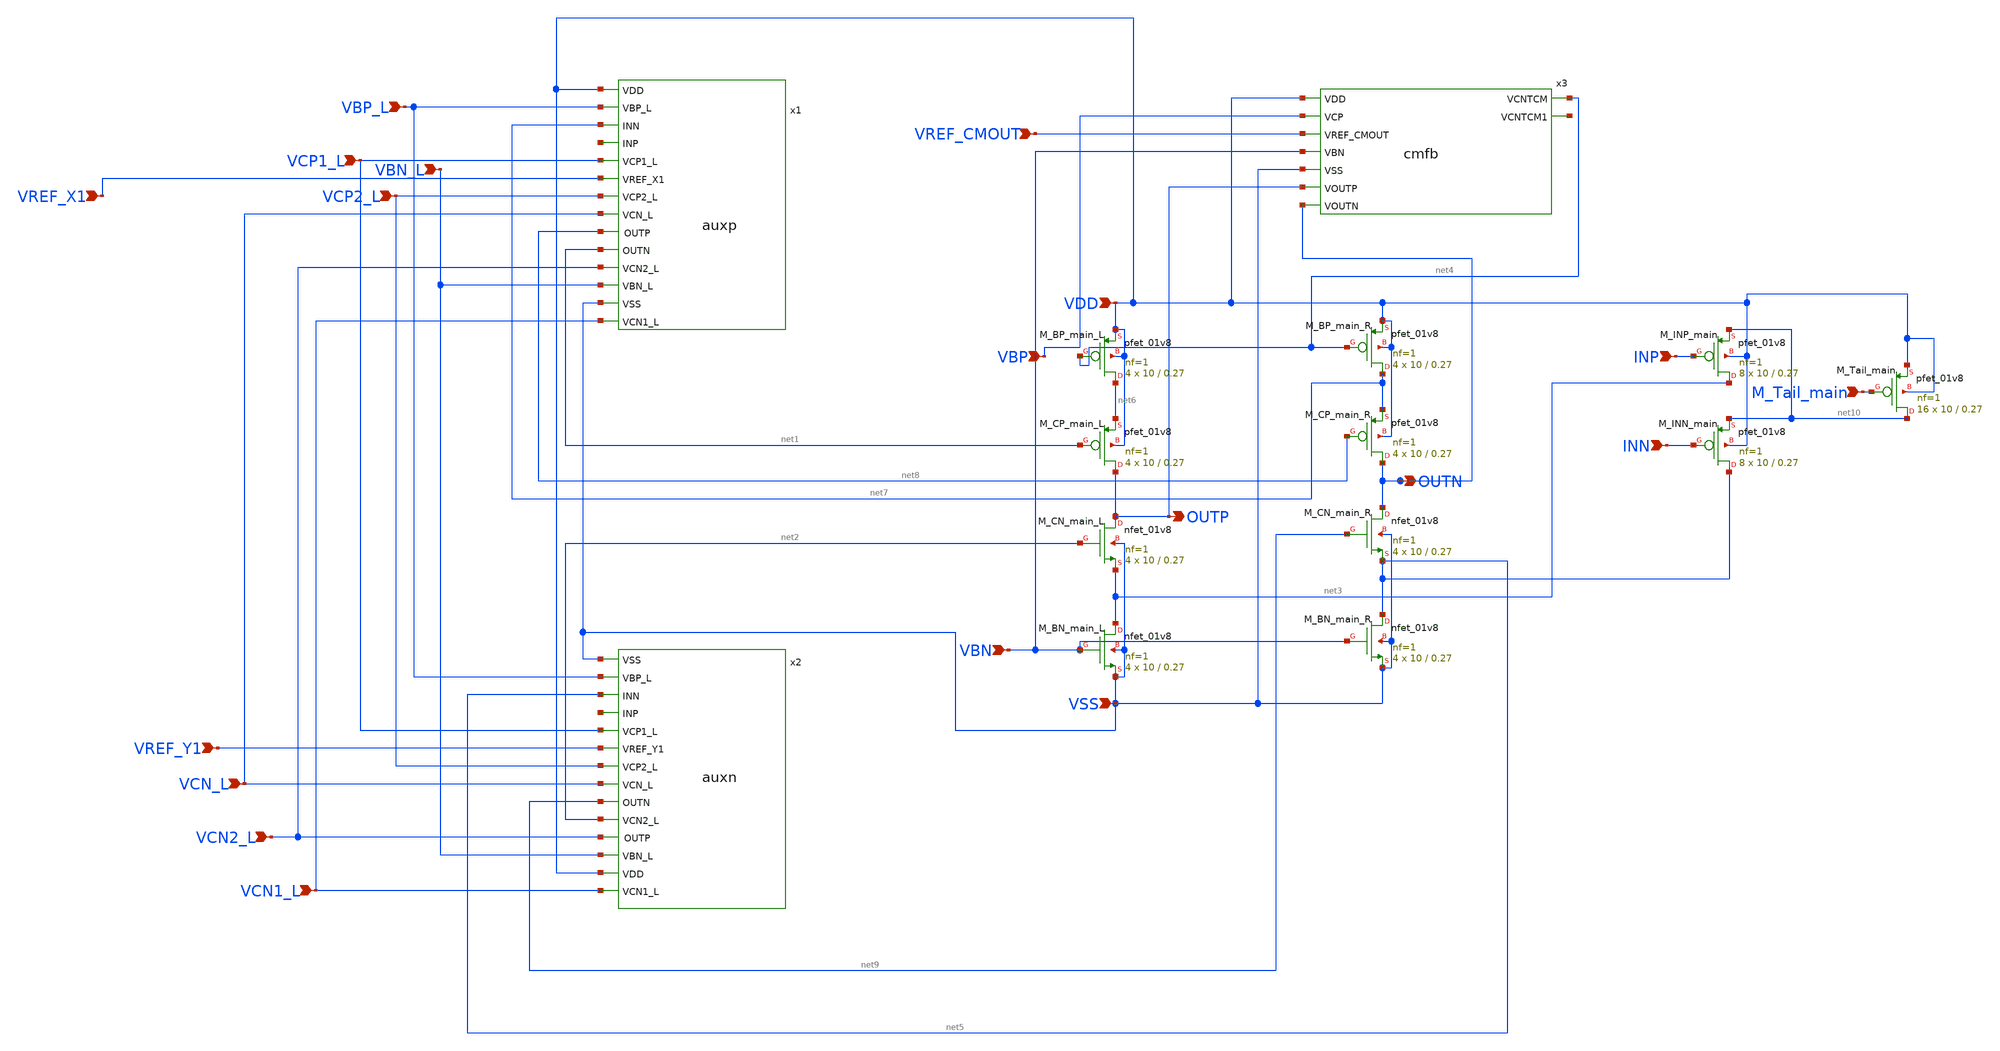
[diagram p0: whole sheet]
** sch_path: main_opamp.sch
**.subckt main_opamp INP VDD VSS INN VREF_CMOUT OUTP OUTN VBP VBN M_Tail_main VBP_L VCN1_L VCN2_L
*+ VCN_L VCP2_L VCP1_L VBN_L VREF_X1 VREF_Y1
*.ipin INP
*.ipin VDD
*.ipin VSS
*.ipin INN
*.ipin VREF_CMOUT
*.opin OUTP
*.opin OUTN
*.ipin VBP
*.ipin VBN
*.ipin M_Tail_main
*.ipin VBP_L
*.ipin VCN1_L
*.ipin VCN2_L
*.ipin VCN_L
*.ipin VCP2_L
*.ipin VCP1_L
*.ipin VBN_L
*.ipin VREF_X1
*.ipin VREF_Y1
x3 VDD VBP net4 net11 VREF_CMOUT VBN VSS OUTP OUTN cmfb
XM_BP_main_L net6 net4 VDD VDD sky130_fd_pr__pfet_01v8 L=0.27 W=10 nf=1 ad='int((1 + 1)/2) * 10 / 1 * 0.29'
+ as='int((1 + 2)/2) * 10 / 1 * 0.29' pd='2*int((1 + 1)/2) * (10 / 1 + 0.29)' ps='2*int((1 + 2)/2) * (10 / 1 + 0.29)'
+ nrd='0.29 / 10 ' nrs='0.29 / 10 ' sa=0 sb=0 sd=0 mult=4 m=4
XM_CP_main_L OUTP net1 net6 VDD sky130_fd_pr__pfet_01v8 L=0.27 W=10 nf=1 ad='int((1 + 1)/2) * 10 / 1 * 0.29'
+ as='int((1 + 2)/2) * 10 / 1 * 0.29' pd='2*int((1 + 1)/2) * (10 / 1 + 0.29)' ps='2*int((1 + 2)/2) * (10 / 1 + 0.29)'
+ nrd='0.29 / 10 ' nrs='0.29 / 10 ' sa=0 sb=0 sd=0 mult=4 m=4
XM_CN_main_L OUTP net2 net3 VSS sky130_fd_pr__nfet_01v8 L=0.27 W=10 nf=1 ad='int((1 + 1)/2) * 10 / 1 * 0.29'
+ as='int((1 + 2)/2) * 10 / 1 * 0.29' pd='2*int((1 + 1)/2) * (10 / 1 + 0.29)' ps='2*int((1 + 2)/2) * (10 / 1 + 0.29)'
+ nrd='0.29 / 10 ' nrs='0.29 / 10 ' sa=0 sb=0 sd=0 mult=4 m=4
XM_BN_main_L net3 VBN VSS VSS sky130_fd_pr__nfet_01v8 L=0.27 W=10 nf=1 ad='int((1 + 1)/2) * 10 / 1 * 0.29'
+ as='int((1 + 2)/2) * 10 / 1 * 0.29' pd='2*int((1 + 1)/2) * (10 / 1 + 0.29)' ps='2*int((1 + 2)/2) * (10 / 1 + 0.29)'
+ nrd='0.29 / 10 ' nrs='0.29 / 10 ' sa=0 sb=0 sd=0 mult=4 m=4
XM_BP_main_R net7 net4 VDD VDD sky130_fd_pr__pfet_01v8 L=0.27 W=10 nf=1 ad='int((1 + 1)/2) * 10 / 1 * 0.29'
+ as='int((1 + 2)/2) * 10 / 1 * 0.29' pd='2*int((1 + 1)/2) * (10 / 1 + 0.29)' ps='2*int((1 + 2)/2) * (10 / 1 + 0.29)'
+ nrd='0.29 / 10 ' nrs='0.29 / 10 ' sa=0 sb=0 sd=0 mult=4 m=4
XM_CP_main_R OUTN net8 net7 VDD sky130_fd_pr__pfet_01v8 L=0.27 W=10 nf=1 ad='int((1 + 1)/2) * 10 / 1 * 0.29'
+ as='int((1 + 2)/2) * 10 / 1 * 0.29' pd='2*int((1 + 1)/2) * (10 / 1 + 0.29)' ps='2*int((1 + 2)/2) * (10 / 1 + 0.29)'
+ nrd='0.29 / 10 ' nrs='0.29 / 10 ' sa=0 sb=0 sd=0 mult=4 m=4
XM_CN_main_R OUTN net9 net5 VSS sky130_fd_pr__nfet_01v8 L=0.27 W=10 nf=1 ad='int((1 + 1)/2) * 10 / 1 * 0.29'
+ as='int((1 + 2)/2) * 10 / 1 * 0.29' pd='2*int((1 + 1)/2) * (10 / 1 + 0.29)' ps='2*int((1 + 2)/2) * (10 / 1 + 0.29)'
+ nrd='0.29 / 10 ' nrs='0.29 / 10 ' sa=0 sb=0 sd=0 mult=4 m=4
XM_BN_main_R net5 VBN VSS VSS sky130_fd_pr__nfet_01v8 L=0.27 W=10 nf=1 ad='int((1 + 1)/2) * 10 / 1 * 0.29'
+ as='int((1 + 2)/2) * 10 / 1 * 0.29' pd='2*int((1 + 1)/2) * (10 / 1 + 0.29)' ps='2*int((1 + 2)/2) * (10 / 1 + 0.29)'
+ nrd='0.29 / 10 ' nrs='0.29 / 10 ' sa=0 sb=0 sd=0 mult=4 m=4
XM_INP_main net3 INP net10 VDD sky130_fd_pr__pfet_01v8 L=0.27 W=10 nf=1 ad='int((1 + 1)/2) * 10 / 1 * 0.29'
+ as='int((1 + 2)/2) * 10 / 1 * 0.29' pd='2*int((1 + 1)/2) * (10 / 1 + 0.29)' ps='2*int((1 + 2)/2) * (10 / 1 + 0.29)'
+ nrd='0.29 / 10 ' nrs='0.29 / 10 ' sa=0 sb=0 sd=0 mult=8 m=8
XM_INN_main net5 INN net10 VDD sky130_fd_pr__pfet_01v8 L=0.27 W=10 nf=1 ad='int((1 + 1)/2) * 10 / 1 * 0.29'
+ as='int((1 + 2)/2) * 10 / 1 * 0.29' pd='2*int((1 + 1)/2) * (10 / 1 + 0.29)' ps='2*int((1 + 2)/2) * (10 / 1 + 0.29)'
+ nrd='0.29 / 10 ' nrs='0.29 / 10 ' sa=0 sb=0 sd=0 mult=8 m=8
XM_Tail_main net10 M_Tail_main VDD VDD sky130_fd_pr__pfet_01v8 L=0.27 W=10 nf=1 ad='int((1 + 1)/2) * 10 / 1 * 0.29'
+ as='int((1 + 2)/2) * 10 / 1 * 0.29' pd='2*int((1 + 1)/2) * (10 / 1 + 0.29)' ps='2*int((1 + 2)/2) * (10 / 1 + 0.29)'
+ nrd='0.29 / 10 ' nrs='0.29 / 10 ' sa=0 sb=0 sd=0 mult=16 m=16
x2 VSS VBP_L net5 net12 VCP1_L VREF_Y1 VCP2_L VCN_L net9 VCN2_L net2 VBN_L VDD VCN1_L auxn
x1 VDD VBP_L net7 net13 VCP1_L VREF_X1 VCP2_L VCN_L net8 net1 VCN2_L VBN_L VSS VCN1_L auxp
**.ends

* expanding   symbol:  cmfb.sym # of pins=9
** sym_path: cmfb.sym
** sch_path: cmfb.sch
.subckt cmfb VDD VCP VCNTCM VCNTCM1 VREF_CMOUT VBN VSS VOUTP VOUTN
*.ipin VDD
*.ipin VSS
*.ipin VOUTP
*.ipin VOUTN
*.ipin VBN
*.ipin VCP
*.ipin VREF_CMOUT
*.opin VCNTCM
*.opin VCNTCM1
XR1 VOUTN CM sky130_fd_pr__res_generic_po W=48.2 L=100000 m=1
XR2 VOUTP CM sky130_fd_pr__res_generic_po W=48.2 L=100000 m=1
XC1 CM VOUTN sky130_fd_pr__cap_mim_m3_1 W=31.62 L=31.62 MF=1 m=1
XC2 CM VOUTP sky130_fd_pr__cap_mim_m3_1 W=31.62 L=31.62 MF=1 m=1
XM_CM VCNTCM CM net1 VSS sky130_fd_pr__nfet_01v8 L=0.27 W=10 nf=1 ad='int((1 + 1)/2) * 10 / 1 * 0.29'
+ as='int((1 + 2)/2) * 10 / 1 * 0.29' pd='2*int((1 + 1)/2) * (10 / 1 + 0.29)' ps='2*int((1 + 2)/2) * (10 / 1 + 0.29)'
+ nrd='0.29 / 10 ' nrs='0.29 / 10 ' sa=0 sb=0 sd=0 mult=1 m=1
XM_CM1 VCNTCM1 VREF_CMOUT net1 VSS sky130_fd_pr__nfet_01v8 L=0.27 W=10 nf=1 ad='int((1 + 1)/2) * 10 / 1 * 0.29'
+ as='int((1 + 2)/2) * 10 / 1 * 0.29' pd='2*int((1 + 1)/2) * (10 / 1 + 0.29)' ps='2*int((1 + 2)/2) * (10 / 1 + 0.29)'
+ nrd='0.29 / 10 ' nrs='0.29 / 10 ' sa=0 sb=0 sd=0 mult=1 m=1
XM_BN net1 VBN VSS VSS sky130_fd_pr__nfet_01v8 L=0.27 W=10 nf=1 ad='int((1 + 1)/2) * 10 / 1 * 0.29' as='int((1 + 2)/2) * 10 / 1 * 0.29'
+ pd='2*int((1 + 1)/2) * (10 / 1 + 0.29)' ps='2*int((1 + 2)/2) * (10 / 1 + 0.29)' nrd='0.29 / 10 ' nrs='0.29 / 10 '
+ sa=0 sb=0 sd=0 mult=1 m=1
XM_CMP net2 C VDD VDD sky130_fd_pr__pfet_01v8 L=0.27 W=10 nf=1 ad='int((1 + 1)/2) * 10 / 1 * 0.29' as='int((1 + 2)/2) * 10 / 1 * 0.29'
+ pd='2*int((1 + 1)/2) * (10 / 1 + 0.29)' ps='2*int((1 + 2)/2) * (10 / 1 + 0.29)' nrd='0.29 / 10 ' nrs='0.29 / 10 '
+ sa=0 sb=0 sd=0 mult=1 m=1
XM_CMP1 net3 C VDD VDD sky130_fd_pr__pfet_01v8 L=0.27 W=10 nf=1 ad='int((1 + 1)/2) * 10 / 1 * 0.29' as='int((1 + 2)/2) * 10 / 1 * 0.29'
+ pd='2*int((1 + 1)/2) * (10 / 1 + 0.29)' ps='2*int((1 + 2)/2) * (10 / 1 + 0.29)' nrd='0.29 / 10 ' nrs='0.29 / 10 '
+ sa=0 sb=0 sd=0 mult=1 m=1
XM_CCMP VCNTCM VCP net2 VDD sky130_fd_pr__pfet_01v8 L=0.27 W=10 nf=1 ad='int((1 + 1)/2) * 10 / 1 * 0.29'
+ as='int((1 + 2)/2) * 10 / 1 * 0.29' pd='2*int((1 + 1)/2) * (10 / 1 + 0.29)' ps='2*int((1 + 2)/2) * (10 / 1 + 0.29)'
+ nrd='0.29 / 10 ' nrs='0.29 / 10 ' sa=0 sb=0 sd=0 mult=1 m=1
XM_CCMP1 VCNTCM1 VCP net3 VDD sky130_fd_pr__pfet_01v8 L=0.27 W=10 nf=1 ad='int((1 + 1)/2) * 10 / 1 * 0.29'
+ as='int((1 + 2)/2) * 10 / 1 * 0.29' pd='2*int((1 + 1)/2) * (10 / 1 + 0.29)' ps='2*int((1 + 2)/2) * (10 / 1 + 0.29)'
+ nrd='0.29 / 10 ' nrs='0.29 / 10 ' sa=0 sb=0 sd=0 mult=1 m=1
XR3 VCNTCM C sky130_fd_pr__res_generic_po W=48.2 L=15000 m=1
XR4 C VCNTCM1 sky130_fd_pr__res_generic_po W=48.2 L=15000 m=1
.ends


* expanding   symbol:  auxn.sym # of pins=14
** sym_path: auxn.sym
** sch_path: auxn.sch
.subckt auxn VSS VBP_L INN INP VCP1_L VREF_Y1 VCP2_L VCN_L OUTN OUTP VCN2_L VBN_L VDD VCN1_L
*.ipin VDD
*.ipin VSS
*.ipin VBN_L
*.ipin VCN_L
*.ipin VBP_L
*.ipin VREF_Y1
*.ipin INN
*.ipin INP
*.ipin VCP1_L
*.ipin VCP2_L
*.ipin VCN1_L
*.ipin VCN2_L
*.opin OUTP
*.opin OUTN
XM_aux1 p INN net3 VSS sky130_fd_pr__nfet_01v8 L=0.27 W=10 nf=1 ad='int((1 + 1)/2) * 10 / 1 * 0.29' as='int((1 + 2)/2) * 10 / 1 * 0.29'
+ pd='2*int((1 + 1)/2) * (10 / 1 + 0.29)' ps='2*int((1 + 2)/2) * (10 / 1 + 0.29)' nrd='0.29 / 10 ' nrs='0.29 / 10 '
+ sa=0 sb=0 sd=0 mult=1 m=1
XM_CASP1 net1 VCN_L net2 VDD sky130_fd_pr__pfet_01v8 L=0.27 W=10 nf=1 ad='int((1 + 1)/2) * 10 / 1 * 0.29'
+ as='int((1 + 2)/2) * 10 / 1 * 0.29' pd='2*int((1 + 1)/2) * (10 / 1 + 0.29)' ps='2*int((1 + 2)/2) * (10 / 1 + 0.29)'
+ nrd='0.29 / 10 ' nrs='0.29 / 10 ' sa=0 sb=0 sd=0 mult=1 m=1
XM_CPA3_N net8 VCN2_L OUTP VDD sky130_fd_pr__pfet_01v8 L=0.27 W=10 nf=1 ad='int((1 + 1)/2) * 10 / 1 * 0.29'
+ as='int((1 + 2)/2) * 10 / 1 * 0.29' pd='2*int((1 + 1)/2) * (10 / 1 + 0.29)' ps='2*int((1 + 2)/2) * (10 / 1 + 0.29)'
+ nrd='0.29 / 10 ' nrs='0.29 / 10 ' sa=0 sb=0 sd=0 mult=1 m=1
XM_aux2_N p INP net7 VSS sky130_fd_pr__nfet_01v8 L=0.27 W=10 nf=1 ad='int((1 + 1)/2) * 10 / 1 * 0.29'
+ as='int((1 + 2)/2) * 10 / 1 * 0.29' pd='2*int((1 + 1)/2) * (10 / 1 + 0.29)' ps='2*int((1 + 2)/2) * (10 / 1 + 0.29)'
+ nrd='0.29 / 10 ' nrs='0.29 / 10 ' sa=0 sb=0 sd=0 mult=1 m=1
XM_NF2 VSS net1 p VSS sky130_fd_pr__nfet_01v8 L=0.27 W=10 nf=1 ad='int((1 + 1)/2) * 10 / 1 * 0.29' as='int((1 + 2)/2) * 10 / 1 * 0.29'
+ pd='2*int((1 + 1)/2) * (10 / 1 + 0.29)' ps='2*int((1 + 2)/2) * (10 / 1 + 0.29)' nrd='0.29 / 10 ' nrs='0.29 / 10 '
+ sa=0 sb=0 sd=0 mult=3 m=3
XM_BNA2_N VSS VBP_L net9 VSS sky130_fd_pr__nfet_01v8 L=0.27 W=10 nf=1 ad='int((1 + 1)/2) * 10 / 1 * 0.29'
+ as='int((1 + 2)/2) * 10 / 1 * 0.29' pd='2*int((1 + 1)/2) * (10 / 1 + 0.29)' ps='2*int((1 + 2)/2) * (10 / 1 + 0.29)'
+ nrd='0.29 / 10 ' nrs='0.29 / 10 ' sa=0 sb=0 sd=0 mult=1 m=1
XM_CNA4_N net10 VCP2_L OUTP VSS sky130_fd_pr__nfet_01v8 L=0.27 W=10 nf=1 ad='int((1 + 1)/2) * 10 / 1 * 0.29'
+ as='int((1 + 2)/2) * 10 / 1 * 0.29' pd='2*int((1 + 1)/2) * (10 / 1 + 0.29)' ps='2*int((1 + 2)/2) * (10 / 1 + 0.29)'
+ nrd='0.29 / 10 ' nrs='0.29 / 10 ' sa=0 sb=0 sd=0 mult=1 m=1
XM_CPA4_N net7 VCN1_L net8 VDD sky130_fd_pr__pfet_01v8 L=0.27 W=10 nf=1 ad='int((1 + 1)/2) * 10 / 1 * 0.29'
+ as='int((1 + 2)/2) * 10 / 1 * 0.29' pd='2*int((1 + 1)/2) * (10 / 1 + 0.29)' ps='2*int((1 + 2)/2) * (10 / 1 + 0.29)'
+ nrd='0.29 / 10 ' nrs='0.29 / 10 ' sa=0 sb=0 sd=0 mult=1 m=1
XM_BPA3_N VDD VBN_L net7 VDD sky130_fd_pr__pfet_01v8 L=0.27 W=10 nf=1 ad='int((1 + 1)/2) * 10 / 1 * 0.29'
+ as='int((1 + 2)/2) * 10 / 1 * 0.29' pd='2*int((1 + 1)/2) * (10 / 1 + 0.29)' ps='2*int((1 + 2)/2) * (10 / 1 + 0.29)'
+ nrd='0.29 / 10 ' nrs='0.29 / 10 ' sa=0 sb=0 sd=0 mult=2 m=2
XM_NF1 VSS VBP_L net1 VSS sky130_fd_pr__nfet_01v8 L=0.27 W=10 nf=1 ad='int((1 + 1)/2) * 10 / 1 * 0.29'
+ as='int((1 + 2)/2) * 10 / 1 * 0.29' pd='2*int((1 + 1)/2) * (10 / 1 + 0.29)' ps='2*int((1 + 2)/2) * (10 / 1 + 0.29)'
+ nrd='0.29 / 10 ' nrs='0.29 / 10 ' sa=0 sb=0 sd=0 mult=1 m=1
XM_FVF_N p VREF_Y1 net2 VSS sky130_fd_pr__nfet_01v8 L=0.27 W=10 nf=1 ad='int((1 + 1)/2) * 10 / 1 * 0.29'
+ as='int((1 + 2)/2) * 10 / 1 * 0.29' pd='2*int((1 + 1)/2) * (10 / 1 + 0.29)' ps='2*int((1 + 2)/2) * (10 / 1 + 0.29)'
+ nrd='0.29 / 10 ' nrs='0.29 / 10 ' sa=0 sb=0 sd=0 mult=1 m=1
XM_BPA_core VDD VBN_L net2 VDD sky130_fd_pr__pfet_01v8 L=0.27 W=10 nf=1 ad='int((1 + 1)/2) * 10 / 1 * 0.29'
+ as='int((1 + 2)/2) * 10 / 1 * 0.29' pd='2*int((1 + 1)/2) * (10 / 1 + 0.29)' ps='2*int((1 + 2)/2) * (10 / 1 + 0.29)'
+ nrd='0.29 / 10 ' nrs='0.29 / 10 ' sa=0 sb=0 sd=0 mult=2 m=2
XM_BNA1_N VSS VBP_L net5 VSS sky130_fd_pr__nfet_01v8 L=0.27 W=10 nf=1 ad='int((1 + 1)/2) * 10 / 1 * 0.29'
+ as='int((1 + 2)/2) * 10 / 1 * 0.29' pd='2*int((1 + 1)/2) * (10 / 1 + 0.29)' ps='2*int((1 + 2)/2) * (10 / 1 + 0.29)'
+ nrd='0.29 / 10 ' nrs='0.29 / 10 ' sa=0 sb=0 sd=0 mult=1 m=1
XM_CNA1_N net5 VCP1_L net6 VSS sky130_fd_pr__nfet_01v8 L=0.27 W=10 nf=1 ad='int((1 + 1)/2) * 10 / 1 * 0.29'
+ as='int((1 + 2)/2) * 10 / 1 * 0.29' pd='2*int((1 + 1)/2) * (10 / 1 + 0.29)' ps='2*int((1 + 2)/2) * (10 / 1 + 0.29)'
+ nrd='0.29 / 10 ' nrs='0.29 / 10 ' sa=0 sb=0 sd=0 mult=1 m=1
XM_CNA2_N net6 VCP2_L OUTN VSS sky130_fd_pr__nfet_01v8 L=0.27 W=10 nf=1 ad='int((1 + 1)/2) * 10 / 1 * 0.29'
+ as='int((1 + 2)/2) * 10 / 1 * 0.29' pd='2*int((1 + 1)/2) * (10 / 1 + 0.29)' ps='2*int((1 + 2)/2) * (10 / 1 + 0.29)'
+ nrd='0.29 / 10 ' nrs='0.29 / 10 ' sa=0 sb=0 sd=0 mult=1 m=1
XM_CPA2_N net4 VCN2_L OUTN VDD sky130_fd_pr__pfet_01v8 L=0.27 W=10 nf=1 ad='int((1 + 1)/2) * 10 / 1 * 0.29'
+ as='int((1 + 2)/2) * 10 / 1 * 0.29' pd='2*int((1 + 1)/2) * (10 / 1 + 0.29)' ps='2*int((1 + 2)/2) * (10 / 1 + 0.29)'
+ nrd='0.29 / 10 ' nrs='0.29 / 10 ' sa=0 sb=0 sd=0 mult=1 m=1
XM_CPA1_N net3 VCN1_L net4 VDD sky130_fd_pr__pfet_01v8 L=0.27 W=10 nf=1 ad='int((1 + 1)/2) * 10 / 1 * 0.29'
+ as='int((1 + 2)/2) * 10 / 1 * 0.29' pd='2*int((1 + 1)/2) * (10 / 1 + 0.29)' ps='2*int((1 + 2)/2) * (10 / 1 + 0.29)'
+ nrd='0.29 / 10 ' nrs='0.29 / 10 ' sa=0 sb=0 sd=0 mult=1 m=1
XM_BPA1_N VDD VBN_L net3 VDD sky130_fd_pr__pfet_01v8 L=0.27 W=10 nf=1 ad='int((1 + 1)/2) * 10 / 1 * 0.29'
+ as='int((1 + 2)/2) * 10 / 1 * 0.29' pd='2*int((1 + 1)/2) * (10 / 1 + 0.29)' ps='2*int((1 + 2)/2) * (10 / 1 + 0.29)'
+ nrd='0.29 / 10 ' nrs='0.29 / 10 ' sa=0 sb=0 sd=0 mult=2 m=2
XCauxn net11 VSS sky130_fd_pr__cap_mim_m3_1 W=5.48 L=5.48 MF=2 m=2
XRauxn net11 OUTP sky130_fd_pr__res_generic_po W=1 L=187.5 m=1
XM_BNA1 net9 VCP1_L net10 VSS sky130_fd_pr__nfet_01v8 L=0.27 W=10 nf=1 ad='int((1 + 1)/2) * 10 / 1 * 0.29'
+ as='int((1 + 2)/2) * 10 / 1 * 0.29' pd='2*int((1 + 1)/2) * (10 / 1 + 0.29)' ps='2*int((1 + 2)/2) * (10 / 1 + 0.29)'
+ nrd='0.29 / 10 ' nrs='0.29 / 10 ' sa=0 sb=0 sd=0 mult=1 m=1
.ends


* expanding   symbol:  auxp.sym # of pins=14
** sym_path: auxp.sym
** sch_path: auxp.sch
.subckt auxp VDD VBP_L INN INP VCP1_L VREF_X1 VCP2_L VCN_L OUTP OUTN VCN2_L VBN_L VSS VCN1_L
*.ipin VSS
*.ipin VDD
*.ipin VBN_L
*.ipin VCN_L
*.ipin VBP_L
*.ipin VREF_X1
*.ipin INN
*.ipin INP
*.ipin VCP1_L
*.ipin VCP2_L
*.ipin VCN1_L
*.ipin VCN2_L
*.opin OUTP
*.opin OUTN
XM_BNA2 net2 VBN_L VSS VSS sky130_fd_pr__nfet_01v8 L=0.27 W=10 nf=1 ad='int((1 + 1)/2) * 10 / 1 * 0.29'
+ as='int((1 + 2)/2) * 10 / 1 * 0.29' pd='2*int((1 + 1)/2) * (10 / 1 + 0.29)' ps='2*int((1 + 2)/2) * (10 / 1 + 0.29)'
+ nrd='0.29 / 10 ' nrs='0.29 / 10 ' sa=0 sb=0 sd=0 mult=2 m=2
XM_FVF net2 VREF_X1 p VDD sky130_fd_pr__pfet_01v8 L=0.27 W=10 nf=1 ad='int((1 + 1)/2) * 10 / 1 * 0.29'
+ as='int((1 + 2)/2) * 10 / 1 * 0.29' pd='2*int((1 + 1)/2) * (10 / 1 + 0.29)' ps='2*int((1 + 2)/2) * (10 / 1 + 0.29)'
+ nrd='0.29 / 10 ' nrs='0.29 / 10 ' sa=0 sb=0 sd=0 mult=1 m=1
XM_PF1 net1 VBP_L VDD VDD sky130_fd_pr__pfet_01v8 L=0.27 W=10 nf=1 ad='int((1 + 1)/2) * 10 / 1 * 0.29'
+ as='int((1 + 2)/2) * 10 / 1 * 0.29' pd='2*int((1 + 1)/2) * (10 / 1 + 0.29)' ps='2*int((1 + 2)/2) * (10 / 1 + 0.29)'
+ nrd='0.29 / 10 ' nrs='0.29 / 10 ' sa=0 sb=0 sd=0 mult=1 m=1
XM_PF2 p net1 VDD VDD sky130_fd_pr__pfet_01v8 L=0.27 W=10 nf=1 ad='int((1 + 1)/2) * 10 / 1 * 0.29' as='int((1 + 2)/2) * 10 / 1 * 0.29'
+ pd='2*int((1 + 1)/2) * (10 / 1 + 0.29)' ps='2*int((1 + 2)/2) * (10 / 1 + 0.29)' nrd='0.29 / 10 ' nrs='0.29 / 10 '
+ sa=0 sb=0 sd=0 mult=3 m=3
XM_CASN1 net1 VCN_L net2 VSS sky130_fd_pr__nfet_01v8 L=0.27 W=10 nf=1 ad='int((1 + 1)/2) * 10 / 1 * 0.29'
+ as='int((1 + 2)/2) * 10 / 1 * 0.29' pd='2*int((1 + 1)/2) * (10 / 1 + 0.29)' ps='2*int((1 + 2)/2) * (10 / 1 + 0.29)'
+ nrd='0.29 / 10 ' nrs='0.29 / 10 ' sa=0 sb=0 sd=0 mult=1 m=1
XM_aux1 net3 INN p VBP_L sky130_fd_pr__pfet_01v8 L=0.27 W=10 nf=1 ad='int((1 + 1)/2) * 10 / 1 * 0.29'
+ as='int((1 + 2)/2) * 10 / 1 * 0.29' pd='2*int((1 + 1)/2) * (10 / 1 + 0.29)' ps='2*int((1 + 2)/2) * (10 / 1 + 0.29)'
+ nrd='0.29 / 10 ' nrs='0.29 / 10 ' sa=0 sb=0 sd=0 mult=1 m=1
XM_BPA1 net5 VBP_L VDD VDD sky130_fd_pr__pfet_01v8 L=0.27 W=10 nf=1 ad='int((1 + 1)/2) * 10 / 1 * 0.29'
+ as='int((1 + 2)/2) * 10 / 1 * 0.29' pd='2*int((1 + 1)/2) * (10 / 1 + 0.29)' ps='2*int((1 + 2)/2) * (10 / 1 + 0.29)'
+ nrd='0.29 / 10 ' nrs='0.29 / 10 ' sa=0 sb=0 sd=0 mult=1 m=1
XM_CPA1 net6 VCP1_L net5 VDD sky130_fd_pr__pfet_01v8 L=0.27 W=10 nf=1 ad='int((1 + 1)/2) * 10 / 1 * 0.29'
+ as='int((1 + 2)/2) * 10 / 1 * 0.29' pd='2*int((1 + 1)/2) * (10 / 1 + 0.29)' ps='2*int((1 + 2)/2) * (10 / 1 + 0.29)'
+ nrd='0.29 / 10 ' nrs='0.29 / 10 ' sa=0 sb=0 sd=0 mult=1 m=1
XM_CPA2 OUTN VCP2_L net6 VDD sky130_fd_pr__pfet_01v8 L=0.27 W=10 nf=1 ad='int((1 + 1)/2) * 10 / 1 * 0.29'
+ as='int((1 + 2)/2) * 10 / 1 * 0.29' pd='2*int((1 + 1)/2) * (10 / 1 + 0.29)' ps='2*int((1 + 2)/2) * (10 / 1 + 0.29)'
+ nrd='0.29 / 10 ' nrs='0.29 / 10 ' sa=0 sb=0 sd=0 mult=1 m=1
XM_CNA2 OUTN VCN2_L net4 VSS sky130_fd_pr__nfet_01v8 L=0.27 W=10 nf=1 ad='int((1 + 1)/2) * 10 / 1 * 0.29'
+ as='int((1 + 2)/2) * 10 / 1 * 0.29' pd='2*int((1 + 1)/2) * (10 / 1 + 0.29)' ps='2*int((1 + 2)/2) * (10 / 1 + 0.29)'
+ nrd='0.29 / 10 ' nrs='0.29 / 10 ' sa=0 sb=0 sd=0 mult=1 m=1
XM_CNA1 net4 VCN1_L net3 VSS sky130_fd_pr__nfet_01v8 L=0.27 W=10 nf=1 ad='int((1 + 1)/2) * 10 / 1 * 0.29'
+ as='int((1 + 2)/2) * 10 / 1 * 0.29' pd='2*int((1 + 1)/2) * (10 / 1 + 0.29)' ps='2*int((1 + 2)/2) * (10 / 1 + 0.29)'
+ nrd='0.29 / 10 ' nrs='0.29 / 10 ' sa=0 sb=0 sd=0 mult=1 m=1
XM_BNA1 net3 VBN_L VSS VSS sky130_fd_pr__nfet_01v8 L=0.27 W=10 nf=1 ad='int((1 + 1)/2) * 10 / 1 * 0.29'
+ as='int((1 + 2)/2) * 10 / 1 * 0.29' pd='2*int((1 + 1)/2) * (10 / 1 + 0.29)' ps='2*int((1 + 2)/2) * (10 / 1 + 0.29)'
+ nrd='0.29 / 10 ' nrs='0.29 / 10 ' sa=0 sb=0 sd=0 mult=2 m=2
XM_aux2 net7 INP p VDD sky130_fd_pr__pfet_01v8 L=0.27 W=10 nf=1 ad='int((1 + 1)/2) * 10 / 1 * 0.29' as='int((1 + 2)/2) * 10 / 1 * 0.29'
+ pd='2*int((1 + 1)/2) * (10 / 1 + 0.29)' ps='2*int((1 + 2)/2) * (10 / 1 + 0.29)' nrd='0.29 / 10 ' nrs='0.29 / 10 '
+ sa=0 sb=0 sd=0 mult=1 m=1
XM_BPA2 net10 VBP_L net9 net9 sky130_fd_pr__pfet_01v8 L=0.27 W=10 nf=1 ad='int((1 + 1)/2) * 10 / 1 * 0.29'
+ as='int((1 + 2)/2) * 10 / 1 * 0.29' pd='2*int((1 + 1)/2) * (10 / 1 + 0.29)' ps='2*int((1 + 2)/2) * (10 / 1 + 0.29)'
+ nrd='0.29 / 10 ' nrs='0.29 / 10 ' sa=0 sb=0 sd=0 mult=1 m=1
XM_CPA3 net11 VCP1_L net10 net9 sky130_fd_pr__pfet_01v8 L=0.27 W=10 nf=1 ad='int((1 + 1)/2) * 10 / 1 * 0.29'
+ as='int((1 + 2)/2) * 10 / 1 * 0.29' pd='2*int((1 + 1)/2) * (10 / 1 + 0.29)' ps='2*int((1 + 2)/2) * (10 / 1 + 0.29)'
+ nrd='0.29 / 10 ' nrs='0.29 / 10 ' sa=0 sb=0 sd=0 mult=1 m=1
XM_CPA4 OUTP VCP2_L net11 net9 sky130_fd_pr__pfet_01v8 L=0.27 W=10 nf=1 ad='int((1 + 1)/2) * 10 / 1 * 0.29'
+ as='int((1 + 2)/2) * 10 / 1 * 0.29' pd='2*int((1 + 1)/2) * (10 / 1 + 0.29)' ps='2*int((1 + 2)/2) * (10 / 1 + 0.29)'
+ nrd='0.29 / 10 ' nrs='0.29 / 10 ' sa=0 sb=0 sd=0 mult=1 m=1
XM_CNA3 OUTP VCN2_L net8 VSS sky130_fd_pr__nfet_01v8 L=0.27 W=10 nf=1 ad='int((1 + 1)/2) * 10 / 1 * 0.29'
+ as='int((1 + 2)/2) * 10 / 1 * 0.29' pd='2*int((1 + 1)/2) * (10 / 1 + 0.29)' ps='2*int((1 + 2)/2) * (10 / 1 + 0.29)'
+ nrd='0.29 / 10 ' nrs='0.29 / 10 ' sa=0 sb=0 sd=0 mult=1 m=1
XM_CNA4 net8 VCN1_L net7 VSS sky130_fd_pr__nfet_01v8 L=0.27 W=10 nf=1 ad='int((1 + 1)/2) * 10 / 1 * 0.29'
+ as='int((1 + 2)/2) * 10 / 1 * 0.29' pd='2*int((1 + 1)/2) * (10 / 1 + 0.29)' ps='2*int((1 + 2)/2) * (10 / 1 + 0.29)'
+ nrd='0.29 / 10 ' nrs='0.29 / 10 ' sa=0 sb=0 sd=0 mult=1 m=1
XM_BNA3 net7 VBN_L VSS VSS sky130_fd_pr__nfet_01v8 L=0.27 W=10 nf=1 ad='int((1 + 1)/2) * 10 / 1 * 0.29'
+ as='int((1 + 2)/2) * 10 / 1 * 0.29' pd='2*int((1 + 1)/2) * (10 / 1 + 0.29)' ps='2*int((1 + 2)/2) * (10 / 1 + 0.29)'
+ nrd='0.29 / 10 ' nrs='0.29 / 10 ' sa=0 sb=0 sd=0 mult=2 m=2
XCauxn net12 VSS sky130_fd_pr__cap_mim_m3_1 W=5.48 L=5.48 MF=1 m=1
XRauxn net12 OUTP sky130_fd_pr__res_generic_po W=1 L=375 m=1
.ends

.end
